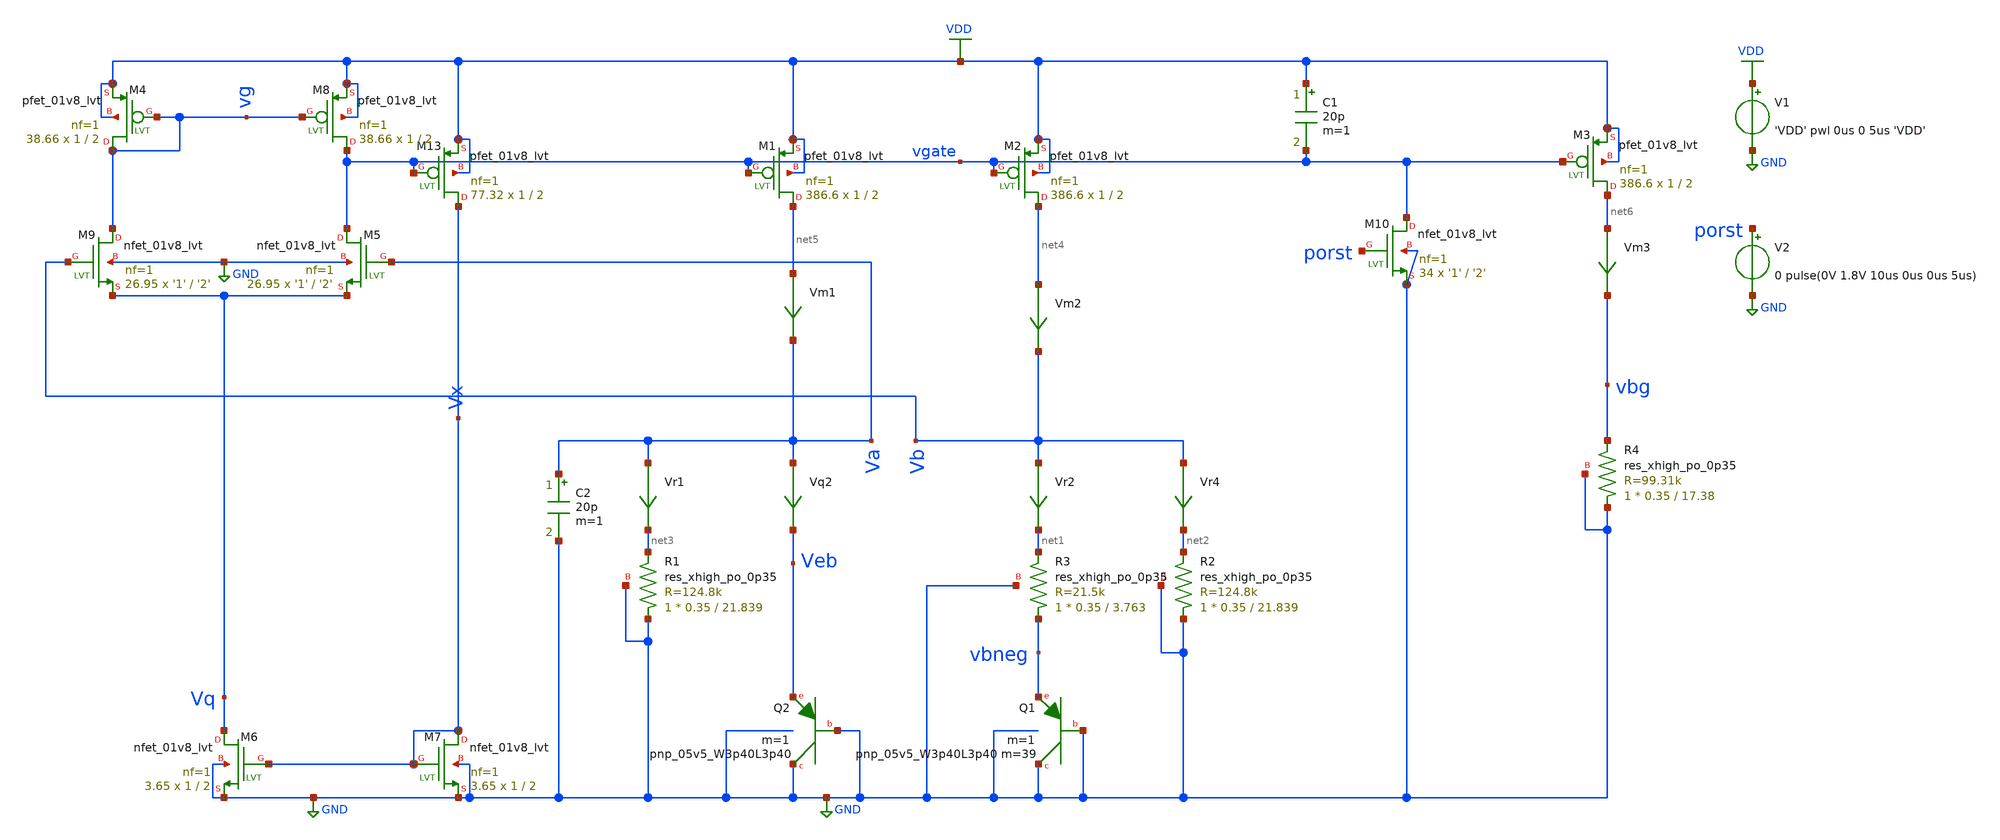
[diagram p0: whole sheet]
** sch_path: schematics/tsmc_bandgap_real_tempsweep.sch
**.subckt tsmc_bandgap_real_tempsweep
V1 VDD GND 'VDD' pwl 0us 0 5us 'VDD'
XQ2 GND GND Veb sky130_fd_pr__pnp_05v5_W3p40L3p40 m=1
Vr4 Vb net2 0
.save i(vr4)
Vr2 Vb net1 0
.save i(vr2)
Vm1 net5 Va 0
.save i(vm1)
Vm2 net4 Vb 0
.save i(vm2)
Vm3 net6 vbg 0
.save i(vm3)
Vr1 Va net3 0
.save i(vr1)
Vq2 Va Veb 0
.save i(vq2)
XQ1 GND GND vbneg sky130_fd_pr__pnp_05v5_W3p40L3p40 m=39 m=1
XM5 vgate Va Vq GND sky130_fd_pr__nfet_01v8_lvt L='2' W='1' nf=1 ad='int((nf+1)/2) * W/nf * 0.29' as='int((nf+2)/2) * W/nf * 0.29'
+ pd='2*int((nf+1)/2) * (W/nf + 0.29)' ps='2*int((nf+2)/2) * (W/nf + 0.29)' nrd='0.29 / W' nrs='0.29 / W'
+ sa=0 sb=0 sd=0 mult=26.95 m=26.95
XM6 Vq Vx GND GND sky130_fd_pr__nfet_01v8_lvt L=2 W=1 nf=1 ad='int((nf+1)/2) * W/nf * 0.29' as='int((nf+2)/2) * W/nf * 0.29'
+ pd='2*int((nf+1)/2) * (W/nf + 0.29)' ps='2*int((nf+2)/2) * (W/nf + 0.29)' nrd='0.29 / W' nrs='0.29 / W'
+ sa=0 sb=0 sd=0 mult=3.65 m=3.65
XM9 vg Vb Vq GND sky130_fd_pr__nfet_01v8_lvt L='2' W='1' nf=1 ad='int((nf+1)/2) * W/nf * 0.29' as='int((nf+2)/2) * W/nf * 0.29'
+ pd='2*int((nf+1)/2) * (W/nf + 0.29)' ps='2*int((nf+2)/2) * (W/nf + 0.29)' nrd='0.29 / W' nrs='0.29 / W'
+ sa=0 sb=0 sd=0 mult=26.95 m=26.95
XM7 Vx Vx GND GND sky130_fd_pr__nfet_01v8_lvt L=2 W=1 nf=1 ad='int((nf+1)/2) * W/nf * 0.29' as='int((nf+2)/2) * W/nf * 0.29'
+ pd='2*int((nf+1)/2) * (W/nf + 0.29)' ps='2*int((nf+2)/2) * (W/nf + 0.29)' nrd='0.29 / W' nrs='0.29 / W'
+ sa=0 sb=0 sd=0 mult=3.65 m=3.65
XM13 Vx vgate VDD VDD sky130_fd_pr__pfet_01v8_lvt L=2 W=1 nf=1 ad='int((nf+1)/2) * W/nf * 0.29' as='int((nf+2)/2) * W/nf * 0.29'
+ pd='2*int((nf+1)/2) * (W/nf + 0.29)' ps='2*int((nf+2)/2) * (W/nf + 0.29)' nrd='0.29 / W' nrs='0.29 / W'
+ sa=0 sb=0 sd=0 mult=77.32 m=77.32
XM1 net5 vgate VDD VDD sky130_fd_pr__pfet_01v8_lvt L=2 W=1 nf=1 ad='int((nf+1)/2) * W/nf * 0.29' as='int((nf+2)/2) * W/nf * 0.29'
+ pd='2*int((nf+1)/2) * (W/nf + 0.29)' ps='2*int((nf+2)/2) * (W/nf + 0.29)' nrd='0.29 / W' nrs='0.29 / W'
+ sa=0 sb=0 sd=0 mult=386.6 m=386.6
XM2 net4 vgate VDD VDD sky130_fd_pr__pfet_01v8_lvt L=2 W=1 nf=1 ad='int((nf+1)/2) * W/nf * 0.29' as='int((nf+2)/2) * W/nf * 0.29'
+ pd='2*int((nf+1)/2) * (W/nf + 0.29)' ps='2*int((nf+2)/2) * (W/nf + 0.29)' nrd='0.29 / W' nrs='0.29 / W'
+ sa=0 sb=0 sd=0 mult=386.6 m=386.6
XM3 net6 vgate VDD VDD sky130_fd_pr__pfet_01v8_lvt L=2 W=1 nf=1 ad='int((nf+1)/2) * W/nf * 0.29' as='int((nf+2)/2) * W/nf * 0.29'
+ pd='2*int((nf+1)/2) * (W/nf + 0.29)' ps='2*int((nf+2)/2) * (W/nf + 0.29)' nrd='0.29 / W' nrs='0.29 / W'
+ sa=0 sb=0 sd=0 mult=386.6 m=386.6
XR1 GND net3 GND sky130_fd_pr__res_xhigh_po_0p35 L=21.839 mult=1 m=1
XR2 GND net2 GND sky130_fd_pr__res_xhigh_po_0p35 L=21.839 mult=1 m=1
XR3 vbneg net1 GND sky130_fd_pr__res_xhigh_po_0p35 L=3.763 mult=1 m=1
XR4 GND vbg GND sky130_fd_pr__res_xhigh_po_0p35 L=17.38 mult=1 m=1
XM4 vg vg VDD VDD sky130_fd_pr__pfet_01v8_lvt L=2 W=1 nf=1 ad='int((nf+1)/2) * W/nf * 0.29' as='int((nf+2)/2) * W/nf * 0.29'
+ pd='2*int((nf+1)/2) * (W/nf + 0.29)' ps='2*int((nf+2)/2) * (W/nf + 0.29)' nrd='0.29 / W' nrs='0.29 / W'
+ sa=0 sb=0 sd=0 mult=38.66 m=38.66
XM8 vgate vg VDD VDD sky130_fd_pr__pfet_01v8_lvt L=2 W=1 nf=1 ad='int((nf+1)/2) * W/nf * 0.29' as='int((nf+2)/2) * W/nf * 0.29'
+ pd='2*int((nf+1)/2) * (W/nf + 0.29)' ps='2*int((nf+2)/2) * (W/nf + 0.29)' nrd='0.29 / W' nrs='0.29 / W'
+ sa=0 sb=0 sd=0 mult=38.66 m=38.66
XM10 vgate porst GND GND sky130_fd_pr__nfet_01v8_lvt L='2' W='1' nf=1 ad='int((nf+1)/2) * W/nf * 0.29'
+ as='int((nf+2)/2) * W/nf * 0.29' pd='2*int((nf+1)/2) * (W/nf + 0.29)' ps='2*int((nf+2)/2) * (W/nf + 0.29)'
+ nrd='0.29 / W' nrs='0.29 / W' sa=0 sb=0 sd=0 mult=34 m=34
V2 porst GND 0 pulse(0V 1.8V 10us 0us 0us 5us)
C1 VDD vgate 20p m=1
C2 Va GND 20p m=1
**** begin user architecture code

.include $::SKYWATER_MODELS/cells/nfet_01v8/sky130_fd_pr__nfet_01v8__tt.corner.spice
.include $::SKYWATER_MODELS/cells/nfet_01v8_lvt/sky130_fd_pr__nfet_01v8_lvt__tt.corner.spice
.include $::SKYWATER_MODELS/cells/pfet_01v8/sky130_fd_pr__pfet_01v8__tt.corner.spice
.include $::SKYWATER_MODELS/cells/nfet_03v3_nvt/sky130_fd_pr__nfet_03v3_nvt__tt.corner.spice
.include $::SKYWATER_MODELS/cells/nfet_05v0_nvt/sky130_fd_pr__nfet_05v0_nvt__tt.corner.spice
.include $::SKYWATER_MODELS/cells/esd_nfet_01v8/sky130_fd_pr__esd_nfet_01v8__tt.corner.spice
.include $::SKYWATER_MODELS/cells/pfet_01v8_lvt/sky130_fd_pr__pfet_01v8_lvt__tt.corner.spice
.include $::SKYWATER_MODELS/cells/pfet_01v8_hvt/sky130_fd_pr__pfet_01v8_hvt__tt.corner.spice
.include $::SKYWATER_MODELS/cells/esd_pfet_g5v0d10v5/sky130_fd_pr__esd_pfet_g5v0d10v5__tt.corner.spice
.include $::SKYWATER_MODELS/cells/pfet_g5v0d10v5/sky130_fd_pr__pfet_g5v0d10v5__tt.corner.spice
.include $::SKYWATER_MODELS/cells/pfet_g5v0d16v0/sky130_fd_pr__pfet_g5v0d16v0__tt.corner.spice
.include $::SKYWATER_MODELS/cells/nfet_g5v0d10v5/sky130_fd_pr__nfet_g5v0d10v5__tt.corner.spice
.include $::SKYWATER_MODELS/cells/nfet_g5v0d16v0/sky130_fd_pr__nfet_g5v0d16v0__tt_discrete.corner.spice
.include $::SKYWATER_MODELS/cells/esd_nfet_g5v0d10v5/sky130_fd_pr__esd_nfet_g5v0d10v5__tt.corner.spice
.include $::SKYWATER_MODELS/models/corners/tt/nonfet.spice
* Mismatch parameters
.include $::SKYWATER_MODELS/cells/nfet_01v8/sky130_fd_pr__nfet_01v8__mismatch.corner.spice
.include $::SKYWATER_MODELS/cells/pfet_01v8/sky130_fd_pr__pfet_01v8__mismatch.corner.spice
.include $::SKYWATER_MODELS/cells/nfet_01v8_lvt/sky130_fd_pr__nfet_01v8_lvt__mismatch.corner.spice
.include $::SKYWATER_MODELS/cells/pfet_01v8_lvt/sky130_fd_pr__pfet_01v8_lvt__mismatch.corner.spice
.include $::SKYWATER_MODELS/cells/pfet_01v8_hvt/sky130_fd_pr__pfet_01v8_hvt__mismatch.corner.spice
.include $::SKYWATER_MODELS/cells/nfet_g5v0d10v5/sky130_fd_pr__nfet_g5v0d10v5__mismatch.corner.spice
.include $::SKYWATER_MODELS/cells/pfet_g5v0d10v5/sky130_fd_pr__pfet_g5v0d10v5__mismatch.corner.spice
.include $::SKYWATER_MODELS/cells/nfet_05v0_nvt/sky130_fd_pr__nfet_05v0_nvt__mismatch.corner.spice
.include $::SKYWATER_MODELS/cells/nfet_03v3_nvt/sky130_fd_pr__nfet_03v3_nvt__mismatch.corner.spice
* Resistor$::SKYWATER_MODELS/Capacitor
.include $::SKYWATER_MODELS/models/r+c/res_typical__cap_typical.spice
.include $::SKYWATER_MODELS/models/r+c/res_typical__cap_typical__lin.spice
* Special cells
.include $::SKYWATER_MODELS/models/corners/tt/specialized_cells.spice
* All models
.include $::SKYWATER_MODELS/models/all.spice
.include $::SKYWATER_MODELS/cells/pnp_05v5/sky130_fd_pr__pnp_05v5_W3p40L3p40.model.spice
* Corner
.include $::SKYWATER_MODELS/models/corners/tt/rf.spice



.option savecurrents
.option warn=1
.param VDD=1.8
.param R3val='22.187k'
.param alpha='1'
.param R2R3ratio='5.6555038*alpha'
.param R2val='R3val*R2R3ratio'
.param R4R2ratio=0.79694273
.param R4val='R2val*R4R2ratio'
.nodeset v(vgate)=1.3
.option temp=0
.dc temp -10 80 10m
.control
save all  @m.xm13.msky130_fd_pr__pfet_01v8_lvt[gm]  @m.xm3.msky130_fd_pr__pfet_01v8_lvt[gm]
+  @m.xm4.msky130_fd_pr__pfet_01v8_lvt[gm]  @m.xm5.msky130_fd_pr__nfet_01v8_lvt[gm]  @m.xm6.msky130_fd_pr__nfet_01v8_lvt[gm]
+  @m.xm7.msky130_fd_pr__nfet_01v8_lvt[gm]  @m.xm8.msky130_fd_pr__pfet_01v8_lvt[gm]  @m.xm9.msky130_fd_pr__nfet_01v8_lvt[gm]
run
*plot Vbg
*plot deriv(Vbg)
save vbg deriv(vbg)
let i = vm3#branch
let indx27 = 3700
let indx0 = 1000
let indx70 = 8000
*indx is the index of temperature sweep for 27degC
echo 'Vbg @ 27degC'
let vbg27c = vbg[indx27]
print vbg27c
echo 'dVbe/degC & ppm @ 27degC'
print deriv(vbg)[indx27] deriv(vbg)[indx27]/vbg27c
echo 'ppm real'
print (vbg[indx70]-vbg[indx0])/vbg[indx27]/(70-0)*1e6
*plot deriv(vbg)/vbg27c
*plot v(va, vb) vs i
*plot vm1#branch vm2#branch vm3#branch
save deriv(vbg)/vbg27c
let vsg = vdd - vgate
let vsd1 = vdd - va
let vsd2 = vdd - vb
let vsd3 = vdd - vbg
let vthp = @m.xm1.msky130_fd_pr__pfet_01v8_lvt['vth']
let vov = vsg - vthp
*plot vov vsd1 vsd2 vsd3
let deltav = vb - vbneg
let r4 =vbg/vm3#branch
let r1 =va/vr1#branch
let r2 =vb/vr4#branch
let r3 =deltav/vr2#branch
let vptat =(r2/r3*deltav)
let sum = veb+vptat
*plot veb vptat sum
*plot deriv(veb) deriv(vptat)
save veb vptat sum deriv(veb) deriv(vptat)
let gm1=@m.xm1.msky130_fd_pr__pfet_01v8_lvt[gm]
let gm2=@m.xm2.msky130_fd_pr__pfet_01v8_lvt[gm]
let Av2=gm2 * ((r3 + r3/ln(39)) * r2 / (r3 + r3/ln(39) + r2) )
let Av1=gm1 * (r1 * r3/ln(39))/(r1 + r3/ln(39))
*plot Av1 Av2 Av2/Av1
let gm13=@m.xm13.msky130_fd_pr__pfet_01v8_lvt[gm]
let gm3=@m.xm3.msky130_fd_pr__pfet_01v8_lvt[gm]
let gm4=@m.xm4.msky130_fd_pr__pfet_01v8_lvt[gm]
let gm5=@m.xm5.msky130_fd_pr__nfet_01v8_lvt[gm]
let gm6=@m.xm6.msky130_fd_pr__nfet_01v8_lvt[gm]
let gm7=@m.xm7.msky130_fd_pr__nfet_01v8_lvt[gm]
let gm8=@m.xm8.msky130_fd_pr__pfet_01v8_lvt[gm]
let gm9=@m.xm9.msky130_fd_pr__nfet_01v8_lvt[gm]
let vdsat1=2/(gm1/vm1#branch)
let vdsat2=2/(gm2/vm2#branch)
let vdsat3=2/(gm3/vm3#branch)
let vdsat4=2/(gm4/@m.xm4.msky130_fd_pr__pfet_01v8_lvt[id])
let vdsat5=2/(gm5/@m.xm5.msky130_fd_pr__nfet_01v8_lvt[id])
let vdsat6=2/(gm6/@m.xm6.msky130_fd_pr__nfet_01v8_lvt[id])
let vdsat7=2/(gm7/@m.xm7.msky130_fd_pr__nfet_01v8_lvt[id])
let vdsat8=2/(gm8/@m.xm8.msky130_fd_pr__pfet_01v8_lvt[id])
let vdsat9=2/(gm9/@m.xm9.msky130_fd_pr__nfet_01v8_lvt[id])
let vdsat13=2/(gm13/@m.xm13.msky130_fd_pr__pfet_01v8_lvt[id])
save (vdd-va-vdsat1) (vdd-vb-vdsat2) (vdd-vbg-vdsat3)  (vdd-vgate-vdsat4) (vgate-vq-vdsat5)
+ (vq-0-vdsat6)  (vx-0-vdsat7) (vdd-vg-vdsat8) (vg-vq-vdsat9) (vdd-vx-vdsat13)

write
unset askquit
quit
.endc


**** end user architecture code
**.ends
.GLOBAL VDD
.GLOBAL GND
.end
